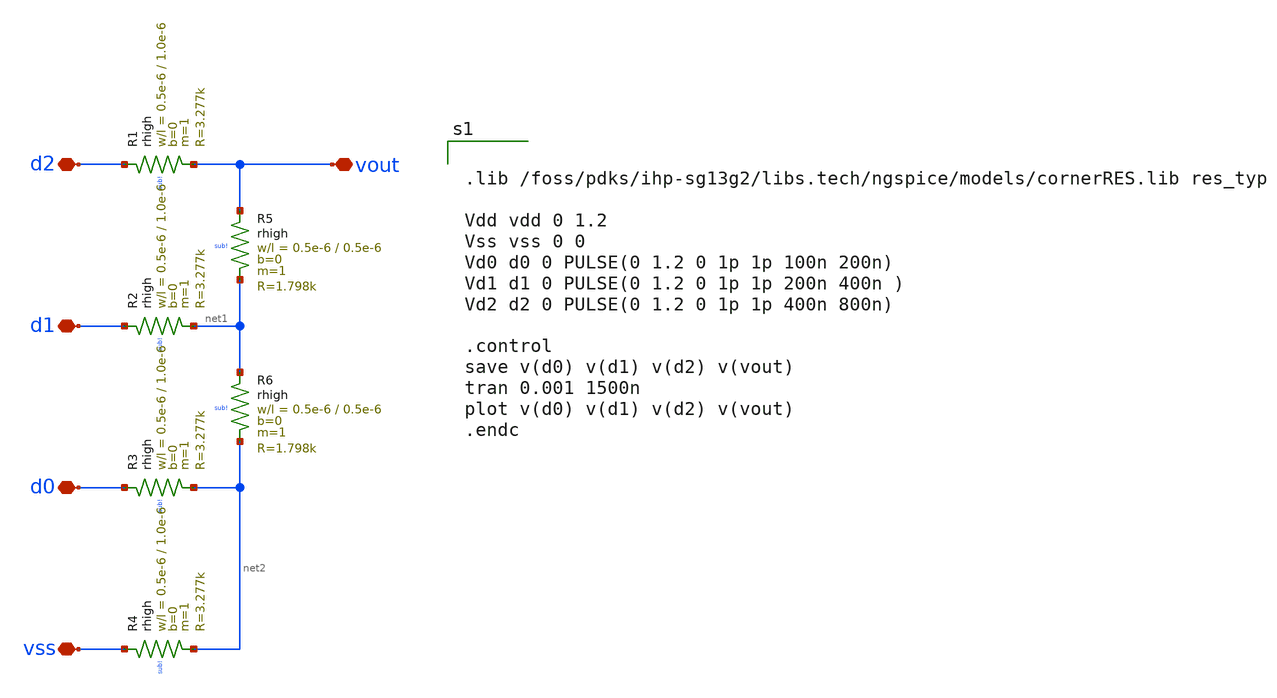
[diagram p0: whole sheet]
** sch_path: xschem/resistor_ladder.sch
**.subckt resistor_ladder vout d0 d1 d2 vss
*.iopin vout
*.iopin d0
*.iopin d1
*.iopin d2
*.iopin vss
XR1 d2 vout sub! rhigh w=0.5e-6 l=1.0e-6 m=1 b=0 mm_ok=1
XR2 d1 net1 sub! rhigh w=0.5e-6 l=1.0e-6 m=1 b=0 mm_ok=1
XR3 d0 net2 sub! rhigh w=0.5e-6 l=1.0e-6 m=1 b=0 mm_ok=1
XR4 vss net2 sub! rhigh w=0.5e-6 l=1.0e-6 m=1 b=0 mm_ok=1
XR5 vout net1 sub! rhigh w=0.5e-6 l=0.5e-6 m=1 b=0 mm_ok=1
XR6 net1 net2 sub! rhigh w=0.5e-6 l=0.5e-6 m=1 b=0 mm_ok=1
**** begin user architecture code


.lib /foss/pdks/ihp-sg13g2/libs.tech/ngspice/models/cornerRES.lib res_typ

Vdd vdd 0 1.2
Vss vss 0 0
Vd0 d0 0 PULSE(0 1.2 0 1p 1p 100n 200n)
Vd1 d1 0 PULSE(0 1.2 0 1p 1p 200n 400n )
Vd2 d2 0 PULSE(0 1.2 0 1p 1p 400n 800n)

.control
save v(d0) v(d1) v(d2) v(vout)
tran 0.001 1500n
plot v(d0) v(d1) v(d2) v(vout)
.endc


**** end user architecture code
**.ends
.end
